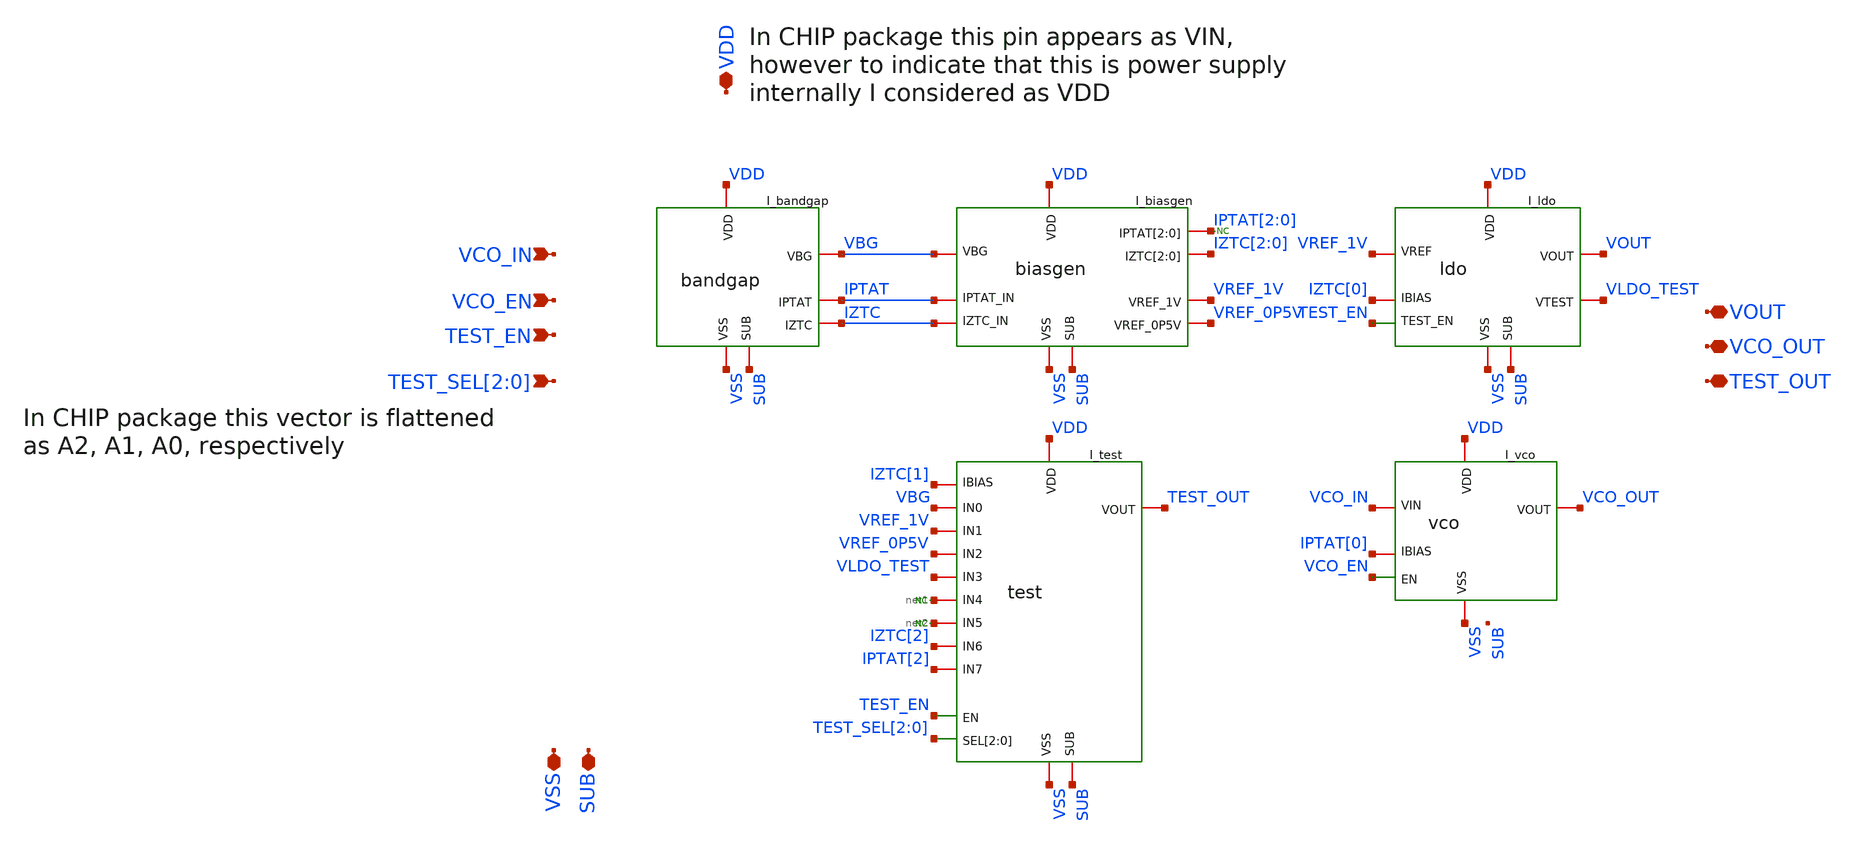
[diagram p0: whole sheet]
** sch_path: designs/libs/core_top/top/top.sch
**.subckt top TEST_SEL[2],TEST_SEL[1],TEST_SEL[0] VCO_IN VDD VSS SUB VOUT VCO_OUT TEST_OUT TEST_EN
*+ VCO_EN
*.ipin TEST_SEL[2],TEST_SEL[1],TEST_SEL[0]
*.ipin VCO_IN
*.iopin VDD
*.iopin VSS
*.iopin SUB
*.iopin VOUT
*.iopin VCO_OUT
*.iopin TEST_OUT
*.ipin TEST_EN
*.ipin VCO_EN
I_bandgap VDD VBG IPTAT IZTC SUB VSS bandgap
I_biasgen VDD VBG IPTAT[2] IPTAT[1] IPTAT[0] IZTC[2] IZTC[1] IZTC[0] IPTAT VREF_1V IZTC VREF_0P5V
+ SUB VSS biasgen
I_ldo VDD VREF_1V VOUT IZTC[0] SUB VSS VLDO_TEST TEST_EN ldo
I_vco VDD IPTAT[0] VCO_OUT VCO_EN VSS VCO_IN vco
I_test VDD IZTC[1] TEST_OUT TEST_EN TEST_SEL[2] TEST_SEL[1] TEST_SEL[0] SUB VSS VBG VREF_1V
+ VREF_0P5V VLDO_TEST net1 net2 IZTC[2] IPTAT[2] test
* noconn #net1
* noconn #net2
* noconn IPTAT[2:0]
**.ends
.end
